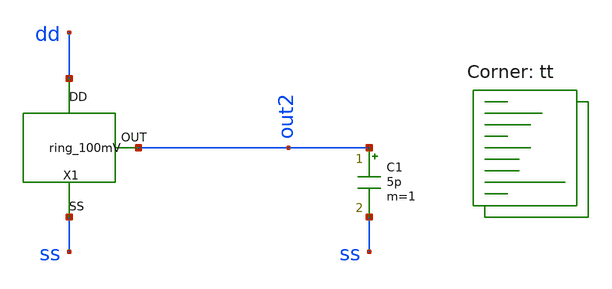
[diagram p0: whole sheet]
** sch_path: xschem/test_ring_100mV.sch
**.subckt test_ring_100mV
X1 out2 dd ss ring_100mV
C1 out2 ss 5p m=1
**** begin user architecture code
.lib $::SKYWATER_MODELS/sky130.lib.spice tt
**** end user architecture code
**.ends

* expanding   symbol:  ring_100mV.sym # of pins=3
** sym_path: xschem/ring_100mV.sym
** sch_path: xschem/ring_100mV.sch
.subckt ring_100mV OUT DD SS
*.iopin DD
*.iopin SS
*.opin OUT
X2 net1 net2 DD SS mdls_inv
X1 net2 net3 DD SS mdls_inv
X3 net3 net4 DD SS mdls_inv
X4 net4 out_aux DD SS mdls_inv
X10 out_aux net5 DD SS mdls_inv
X11 net5 net6 DD SS mdls_inv
X12 net6 net7 DD SS mdls_inv
X13 net7 net8 DD SS mdls_inv
X14 net8 net1 DD SS mdls_inv
X5 out_aux net9 DD SS mdls_inv
X6 net9 OUT DD SS ring_100mV_buffer
.ends


* expanding   symbol:  mdls_inv.sym # of pins=4
** sym_path: xschem/mdls_inv.sym
** sch_path: xschem/mdls_inv.sch
.subckt mdls_inv IN OUT DD SS
*.ipin IN
*.iopin DD
*.iopin SS
*.opin OUT
XM5 OUT IN net1 SS sky130_fd_pr__nfet_01v8_lvt L=0.8 W=5.5 nf=1 ad='int((nf+1)/2) * W/nf * 0.29' as='int((nf+2)/2) * W/nf * 0.29'
+ pd='2*int((nf+1)/2) * (W/nf + 0.29)' ps='2*int((nf+2)/2) * (W/nf + 0.29)' nrd='0.29 / W' nrs='0.29 / W'
+ sa=0 sb=0 sd=0 mult=4 m=4
XM10 OUT IN net2 DD sky130_fd_pr__pfet_01v8_lvt L=0.8 W=1 nf=1 ad='int((nf+1)/2) * W/nf * 0.29' as='int((nf+2)/2) * W/nf * 0.29'
+ pd='2*int((nf+1)/2) * (W/nf + 0.29)' ps='2*int((nf+2)/2) * (W/nf + 0.29)' nrd='0.29 / W' nrs='0.29 / W'
+ sa=0 sb=0 sd=0 mult=1 m=1
XM11 net1 IN SS SS sky130_fd_pr__nfet_01v8_lvt L=1 W=5.5 nf=1 ad='int((nf+1)/2) * W/nf * 0.29' as='int((nf+2)/2) * W/nf * 0.29'
+ pd='2*int((nf+1)/2) * (W/nf + 0.29)' ps='2*int((nf+2)/2) * (W/nf + 0.29)' nrd='0.29 / W' nrs='0.29 / W'
+ sa=0 sb=0 sd=0 mult=2 m=2
XM13 net2 IN DD DD sky130_fd_pr__pfet_01v8_lvt L=2 W=1 nf=1 ad='int((nf+1)/2) * W/nf * 0.29' as='int((nf+2)/2) * W/nf * 0.29'
+ pd='2*int((nf+1)/2) * (W/nf + 0.29)' ps='2*int((nf+2)/2) * (W/nf + 0.29)' nrd='0.29 / W' nrs='0.29 / W'
+ sa=0 sb=0 sd=0 mult=1 m=1
XM1 net1 OUT SS DD sky130_fd_pr__pfet_01v8_lvt L=0.8 W=1 nf=1 ad='int((nf+1)/2) * W/nf * 0.29' as='int((nf+2)/2) * W/nf * 0.29'
+ pd='2*int((nf+1)/2) * (W/nf + 0.29)' ps='2*int((nf+2)/2) * (W/nf + 0.29)' nrd='0.29 / W' nrs='0.29 / W'
+ sa=0 sb=0 sd=0 mult=1 m=1
XM2 net2 OUT DD SS sky130_fd_pr__nfet_01v8_lvt L=0.4 W=5.5 nf=1 ad='int((nf+1)/2) * W/nf * 0.29' as='int((nf+2)/2) * W/nf * 0.29'
+ pd='2*int((nf+1)/2) * (W/nf + 0.29)' ps='2*int((nf+2)/2) * (W/nf + 0.29)' nrd='0.29 / W' nrs='0.29 / W'
+ sa=0 sb=0 sd=0 mult=2 m=2
.ends


* expanding   symbol:  ring_100mV_buffer.sym # of pins=4
** sym_path: xschem/ring_100mV_buffer.sym
** sch_path: xschem/ring_100mV_buffer.sch
.subckt ring_100mV_buffer IN OUT DD SS
*.opin OUT
*.iopin DD
*.iopin SS
*.ipin IN
XM5 net1 IN SS SS sky130_fd_pr__nfet_01v8_lvt L=0.8 W=5.5 nf=1 ad='int((nf+1)/2) * W/nf * 0.29' as='int((nf+2)/2) * W/nf * 0.29'
+ pd='2*int((nf+1)/2) * (W/nf + 0.29)' ps='2*int((nf+2)/2) * (W/nf + 0.29)' nrd='0.29 / W' nrs='0.29 / W'
+ sa=0 sb=0 sd=0 mult=8 m=8
XM10 net1 IN DD DD sky130_fd_pr__pfet_01v8_lvt L=0.8 W=1 nf=1 ad='int((nf+1)/2) * W/nf * 0.29' as='int((nf+2)/2) * W/nf * 0.29'
+ pd='2*int((nf+1)/2) * (W/nf + 0.29)' ps='2*int((nf+2)/2) * (W/nf + 0.29)' nrd='0.29 / W' nrs='0.29 / W'
+ sa=0 sb=0 sd=0 mult=2 m=2
XM1 OUT net1 SS SS sky130_fd_pr__nfet_01v8_lvt L=0.8 W=5.5 nf=1 ad='int((nf+1)/2) * W/nf * 0.29' as='int((nf+2)/2) * W/nf * 0.29'
+ pd='2*int((nf+1)/2) * (W/nf + 0.29)' ps='2*int((nf+2)/2) * (W/nf + 0.29)' nrd='0.29 / W' nrs='0.29 / W'
+ sa=0 sb=0 sd=0 mult=16 m=16
XM2 OUT net1 DD DD sky130_fd_pr__pfet_01v8_lvt L=0.8 W=1 nf=1 ad='int((nf+1)/2) * W/nf * 0.29' as='int((nf+2)/2) * W/nf * 0.29'
+ pd='2*int((nf+1)/2) * (W/nf + 0.29)' ps='2*int((nf+2)/2) * (W/nf + 0.29)' nrd='0.29 / W' nrs='0.29 / W'
+ sa=0 sb=0 sd=0 mult=4 m=4
.ends

**** begin user architecture code


** this experimental option enables mos model bin
** selection based on W/NF instead of W
*.option wnflag=1 savecurrents
.option gmin=1e-14 reltol=1e-3 vntol=1e-4 abstol=1e-14

v_dd dd 0 dc=0.2
v_ss ss 0 dc=0
.ic v(x1.out_aux)=0

.control
  option seed = 1
  let run = 1
  save all
  op
  write test_ring_st.raw
  reset
  set appendwrite
  dowhile run < = 1
    save out1 out2
    tran 0.01m 50m
    write test_ring_st.raw
    let run = run + 1
    reset
  end
  plot out2
.endc


**** end user architecture code
.end
